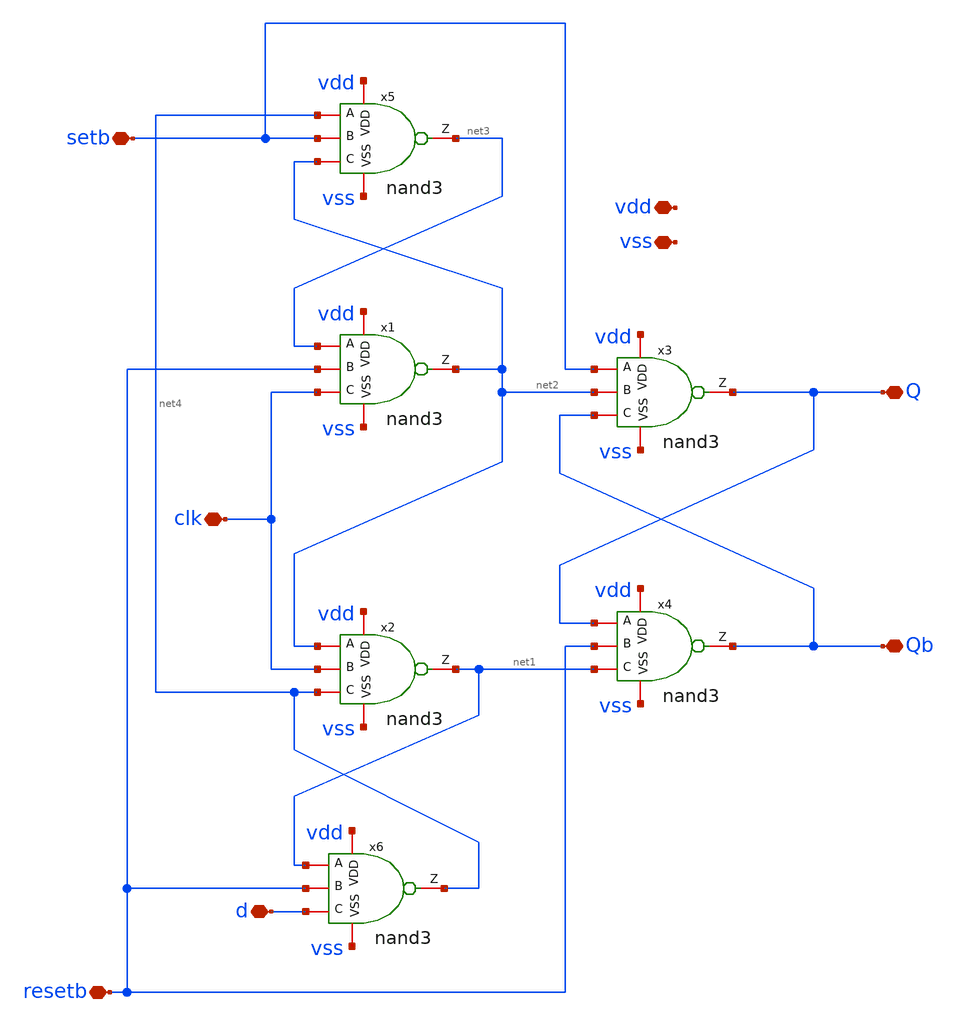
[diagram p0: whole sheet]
** sch_path: designs/libs/SAR_logic/dffrs.sch
**.subckt dffrs vdd vss Q Qb d clk resetb setb
*.iopin vdd
*.iopin vss
*.iopin Q
*.iopin Qb
*.iopin d
*.iopin clk
*.iopin resetb
*.iopin setb
x2 vdd net1 net2 clk net4 vss nand3
x1 vdd net2 net3 resetb clk vss nand3
x3 vdd Q setb net2 Qb vss nand3
x4 vdd Qb Q resetb net1 vss nand3
x5 vdd net3 net4 setb net2 vss nand3
x6 vdd net4 net1 resetb d vss nand3
**.ends
.end
